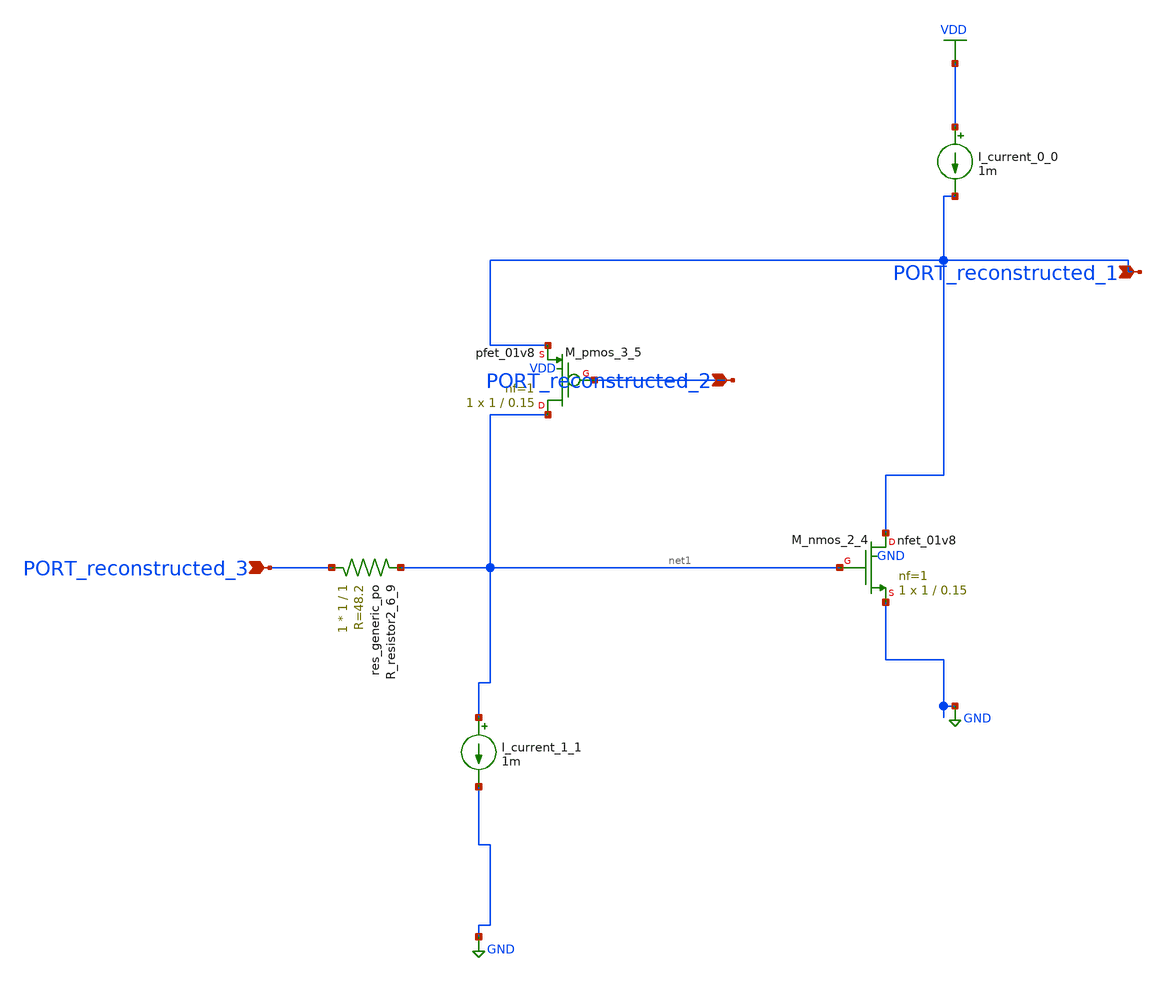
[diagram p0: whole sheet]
** sch_path: schematics/AMSNet/609.sch
**.subckt 609 PORT_reconstructed_2 PORT_reconstructed_1 PORT_reconstructed_3
*.ipin PORT_reconstructed_2
*.ipin PORT_reconstructed_1
*.ipin PORT_reconstructed_3
I_current_0_0 VDD PORT_reconstructed_1 1m
I_current_1_1 net1 GND 1m
XM_nmos_2_4 PORT_reconstructed_1 net1 GND GND sky130_fd_pr__nfet_01v8 L=0.15 W=1 nf=1 ad='int((1 + 1)/2) * 1 / 1 * 0.29'
+ as='int((1 + 2)/2) * 1 / 1 * 0.29' pd='2*int((1 + 1)/2) * (1 / 1 + 0.29)' ps='2*int((1 + 2)/2) * (1 / 1 + 0.29)'
+ nrd='0.29 / 1 ' nrs='0.29 / 1 ' sa=0 sb=0 sd=0 mult=1 m=1
XM_pmos_3_5 net1 PORT_reconstructed_2 PORT_reconstructed_1 VDD sky130_fd_pr__pfet_01v8 L=0.15 W=1 nf=1
+ ad='int((1 + 1)/2) * 1 / 1 * 0.29' as='int((1 + 2)/2) * 1 / 1 * 0.29' pd='2*int((1 + 1)/2) * (1 / 1 + 0.29)'
+ ps='2*int((1 + 2)/2) * (1 / 1 + 0.29)' nrd='0.29 / 1 ' nrs='0.29 / 1 ' sa=0 sb=0 sd=0 mult=1 m=1
XR_resistor2_6_9 PORT_reconstructed_3 net1 sky130_fd_pr__res_generic_po W=1 L=1 m=1
**.ends
.GLOBAL GND
.GLOBAL VDD
.end
